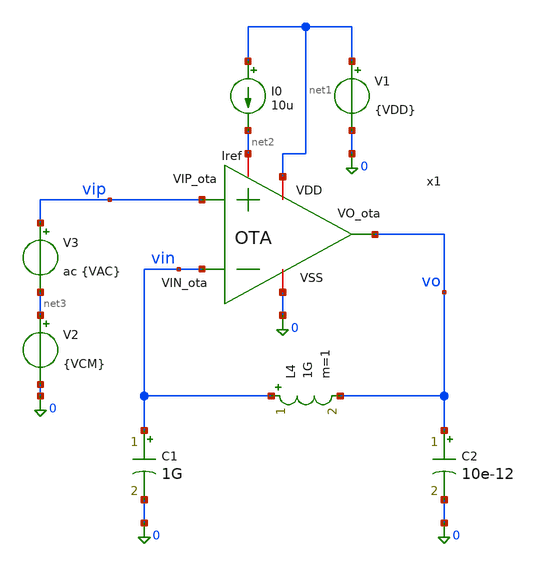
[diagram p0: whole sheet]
** sch_path: xschem/OTA_tb.sch
**.subckt OTA_tb
x1 net1 vo vin vip net2 0 OTA
V1 net1 0 {VDD}
I0 net1 net2 10u
V2 net3 0 {VCM}
V3 vip net3 ac {VAC}
C1 vin 0 1G m=1
L4 vin vo 1G m=1
C2 vo 0 10e-12 m=1
**** begin user architecture code




* 1. Inclusión de libreria de modelos Sky130 PRIMERO
.lib /foss/pdks/sky130A/libs.tech/ngspice/sky130.lib.spice tt

**parametros_ota
.param VDD = 1.8
.param VCM = 0.6
.param VAC = 1



.control

save all
* PMOS
save @m.x1.xMnr.msky130_fd_pr__pfet_01v8[gm]
save @m.x1.xMnr.msky130_fd_pr__pfet_01v8[gds]
save @m.x1.xMnr.msky130_fd_pr__pfet_01v8[id]
save @m.x1.xMnr.msky130_fd_pr__pfet_01v8[vgs]
save @m.x1.xMnr.msky130_fd_pr__pfet_01v8[vds]
save @m.x1.xMnr.msky130_fd_pr__pfet_01v8[vth]
save @m.x1.xMnr.msky130_fd_pr__pfet_01v8[vdsat]

save @m.x1.xMpr.msky130_fd_pr__pfet_01v8[gm]
save @m.x1.xMpr.msky130_fd_pr__pfet_01v8[gds]
save @m.x1.xMpr.msky130_fd_pr__pfet_01v8[id]
save @m.x1.xMpr.msky130_fd_pr__pfet_01v8[vgs]
save @m.x1.xMpr.msky130_fd_pr__pfet_01v8[vds]
save @m.x1.xMpr.msky130_fd_pr__pfet_01v8[vth]
save @m.x1.xMpr.msky130_fd_pr__pfet_01v8[vdsat]

save @m.x1.xMo.msky130_fd_pr__pfet_01v8[gm]
save @m.x1.xMo.msky130_fd_pr__pfet_01v8[gds]
save @m.x1.xMo.msky130_fd_pr__pfet_01v8[id]
save @m.x1.xMo.msky130_fd_pr__pfet_01v8[vgs]
save @m.x1.xMo.msky130_fd_pr__pfet_01v8[vds]
save @m.x1.xMo.msky130_fd_pr__pfet_01v8[vth]
save @m.x1.xMo.msky130_fd_pr__pfet_01v8[vdsat]

* NMOS
save @m.x1.xMn.msky130_fd_pr__nfet_01v8[gm]
save @m.x1.xMn.msky130_fd_pr__nfet_01v8[gds]
save @m.x1.xMn.msky130_fd_pr__nfet_01v8[id]
save @m.x1.xMn.msky130_fd_pr__nfet_01v8[vgs]
save @m.x1.xMn.msky130_fd_pr__nfet_01v8[vds]
save @m.x1.xMn.msky130_fd_pr__nfet_01v8[vth]
save @m.x1.xMn.msky130_fd_pr__nfet_01v8[vdsat]

save @m.x1.xMp.msky130_fd_pr__nfet_01v8[gm]
save @m.x1.xMp.msky130_fd_pr__nfet_01v8[gds]
save @m.x1.xMp.msky130_fd_pr__nfet_01v8[id]
save @m.x1.xMp.msky130_fd_pr__nfet_01v8[vgs]
save @m.x1.xMp.msky130_fd_pr__nfet_01v8[vds]
save @m.x1.xMp.msky130_fd_pr__nfet_01v8[vth]
save @m.x1.xMp.msky130_fd_pr__nfet_01v8[vdsat]

save @m.x1.xMr.msky130_fd_pr__nfet_01v8[gm]
save @m.x1.xMr.msky130_fd_pr__nfet_01v8[gds]
save @m.x1.xMr.msky130_fd_pr__nfet_01v8[id]
save @m.x1.xMr.msky130_fd_pr__nfet_01v8[vgs]
save @m.x1.xMr.msky130_fd_pr__nfet_01v8[vds]
save @m.x1.xMr.msky130_fd_pr__nfet_01v8[vth]
save @m.x1.xMr.msky130_fd_pr__nfet_01v8[vdsat]

save @m.x1.xMrc1.msky130_fd_pr__nfet_01v8[gm]
save @m.x1.xMrc1.msky130_fd_pr__nfet_01v8[gds]
save @m.x1.xMrc1.msky130_fd_pr__nfet_01v8[id]
save @m.x1.xMrc1.msky130_fd_pr__nfet_01v8[vgs]
save @m.x1.xMrc1.msky130_fd_pr__nfet_01v8[vds]
save @m.x1.xMrc1.msky130_fd_pr__nfet_01v8[vth]
save @m.x1.xMrc1.msky130_fd_pr__nfet_01v8[vdsat]

save @m.x1.xMc2.msky130_fd_pr__nfet_01v8[gm]
save @m.x1.xMc2.msky130_fd_pr__nfet_01v8[gds]
save @m.x1.xMc2.msky130_fd_pr__nfet_01v8[id]
save @m.x1.xMc2.msky130_fd_pr__nfet_01v8[vgs]
save @m.x1.xMc2.msky130_fd_pr__nfet_01v8[vds]
save @m.x1.xMc2.msky130_fd_pr__nfet_01v8[vth]
save @m.x1.xMc2.msky130_fd_pr__nfet_01v8[vdsat]

set filetype=ascii
op
write OTA_op.raw


ac dec 10 1 1G
write OTA_ac.raw


* 1. Frecuencia de Corte a -3dB
meas ac f3db WHEN vdb(vo) = vdb(vo)[0] - 3

* 2. UGB (Frecuencia donde la magnitud cruza 0 dB)
meas ac ugb WHEN vdb(vo) = 0

* 3. Crear el vector de fase y convertirlo a grados (multiplicando por 180/pi)
let fase_deg = cph(v(vo)) * 180 / pi

* 4. Medir la fase en grados en el punto exacto del UGB
meas ac fase_ugb FIND fase_deg WHEN vdb(vo) = 0

* 5. Calcular el Margen de Fase automáticamente
let margen_fase = 180 + fase_ugb
print margen_fase

* 6. Graficar la magnitud y la fase ya convertida a grados
plot vdb(vo)
plot fase_deg
.endc


**** end user architecture code
**.ends

* expanding   symbol:  /foss/designs/LDO-sky130/xschem/OTA.sym # of pins=6
** sym_path: xschem/OTA.sym
** sch_path: xschem/OTA.sch
.subckt OTA VDD VO_ota VIN_ota VIP_ota Iref VSS
*.ipin VIN_ota
*.opin VO_ota
*.iopin Iref
*.iopin VSS
*.iopin VDD
*.ipin VIP_ota
XR1 VO_ota1 net1 VDD sky130_fd_pr__res_high_po W=0.35 L=360 mult=1 m=1
XC1 VO_ota net1 sky130_fd_pr__cap_mim_m3_2 W=50 L=50 MF=1 m=1
XMpr VO_ota1 net2 VSS VSS sky130_fd_pr__nfet_01v8 L=0.5 W=3 nf=1 ad='int((1 + 1)/2) * 3 / 1 * 0.29' as='int((1 + 2)/2) * 3 / 1 * 0.29'
+ pd='2*int((1 + 1)/2) * (3 / 1 + 0.29)' ps='2*int((1 + 2)/2) * (3 / 1 + 0.29)' nrd='0.29 / 3 ' nrs='0.29 / 3 '
+ sa=0 sb=0 sd=0 mult=1 m=1
XMnr net2 net2 VSS VSS sky130_fd_pr__nfet_01v8 L=0.5 W=3 nf=1 ad='int((1 + 1)/2) * 3 / 1 * 0.29' as='int((1 + 2)/2) * 3 / 1 * 0.29'
+ pd='2*int((1 + 1)/2) * (3 / 1 + 0.29)' ps='2*int((1 + 2)/2) * (3 / 1 + 0.29)' nrd='0.29 / 3 ' nrs='0.29 / 3 '
+ sa=0 sb=0 sd=0 mult=1 m=1
XMn net2 VIN_ota Vtail VDD sky130_fd_pr__pfet_01v8 L=0.5 W=28 nf=1 ad='int((1 + 1)/2) * 28 / 1 * 0.29'
+ as='int((1 + 2)/2) * 28 / 1 * 0.29' pd='2*int((1 + 1)/2) * (28 / 1 + 0.29)' ps='2*int((1 + 2)/2) * (28 / 1 + 0.29)'
+ nrd='0.29 / 28 ' nrs='0.29 / 28 ' sa=0 sb=0 sd=0 mult=1 m=1
XMp VO_ota1 VIP_ota Vtail VDD sky130_fd_pr__pfet_01v8 L=0.5 W=28 nf=1 ad='int((1 + 1)/2) * 28 / 1 * 0.29'
+ as='int((1 + 2)/2) * 28 / 1 * 0.29' pd='2*int((1 + 1)/2) * (28 / 1 + 0.29)' ps='2*int((1 + 2)/2) * (28 / 1 + 0.29)'
+ nrd='0.29 / 28 ' nrs='0.29 / 28 ' sa=0 sb=0 sd=0 mult=1 m=1
XMo VO_ota VO_ota1 VSS VSS sky130_fd_pr__nfet_01v8 L=0.5 W=3 nf=1 ad='int((1 + 1)/2) * 3 / 1 * 0.29'
+ as='int((1 + 2)/2) * 3 / 1 * 0.29' pd='2*int((1 + 1)/2) * (3 / 1 + 0.29)' ps='2*int((1 + 2)/2) * (3 / 1 + 0.29)'
+ nrd='0.29 / 3 ' nrs='0.29 / 3 ' sa=0 sb=0 sd=0 mult=1 m=1
XMc3 VGP Iref VSS VSS sky130_fd_pr__nfet_01v8 L=0.5 W=1 nf=1 ad='int((1 + 1)/2) * 1 / 1 * 0.29' as='int((1 + 2)/2) * 1 / 1 * 0.29'
+ pd='2*int((1 + 1)/2) * (1 / 1 + 0.29)' ps='2*int((1 + 2)/2) * (1 / 1 + 0.29)' nrd='0.29 / 1 ' nrs='0.29 / 1 '
+ sa=0 sb=0 sd=0 mult=1 m=1
XMp2 Iref Iref VSS VSS sky130_fd_pr__nfet_01v8 L=0.5 W=1 nf=1 ad='int((1 + 1)/2) * 1 / 1 * 0.29' as='int((1 + 2)/2) * 1 / 1 * 0.29'
+ pd='2*int((1 + 1)/2) * (1 / 1 + 0.29)' ps='2*int((1 + 2)/2) * (1 / 1 + 0.29)' nrd='0.29 / 1 ' nrs='0.29 / 1 '
+ sa=0 sb=0 sd=0 mult=1 m=1
XMr VGP VGP VDD VDD sky130_fd_pr__pfet_01v8_lvt L=0.5 W=2.4 nf=1 ad='int((1 + 1)/2) * 2.4 / 1 * 0.29'
+ as='int((1 + 2)/2) * 2.4 / 1 * 0.29' pd='2*int((1 + 1)/2) * (2.4 / 1 + 0.29)' ps='2*int((1 + 2)/2) * (2.4 / 1 + 0.29)'
+ nrd='0.29 / 2.4 ' nrs='0.29 / 2.4 ' sa=0 sb=0 sd=0 mult=1 m=1
XMrc1 Vtail VGP VDD VDD sky130_fd_pr__pfet_01v8_lvt L=0.5 W=19.4 nf=1 ad='int((1 + 1)/2) * 19.4 / 1 * 0.29'
+ as='int((1 + 2)/2) * 19.4 / 1 * 0.29' pd='2*int((1 + 1)/2) * (19.4 / 1 + 0.29)' ps='2*int((1 + 2)/2) * (19.4 / 1 + 0.29)'
+ nrd='0.29 / 19.4 ' nrs='0.29 / 19.4 ' sa=0 sb=0 sd=0 mult=1 m=1
XMrc2 VO_ota VGP VDD VDD sky130_fd_pr__pfet_01v8_lvt L=0.5 W=8 nf=1 ad='int((1 + 1)/2) * 8 / 1 * 0.29'
+ as='int((1 + 2)/2) * 8 / 1 * 0.29' pd='2*int((1 + 1)/2) * (8 / 1 + 0.29)' ps='2*int((1 + 2)/2) * (8 / 1 + 0.29)'
+ nrd='0.29 / 8 ' nrs='0.29 / 8 ' sa=0 sb=0 sd=0 mult=1 m=1
.ends

.end
